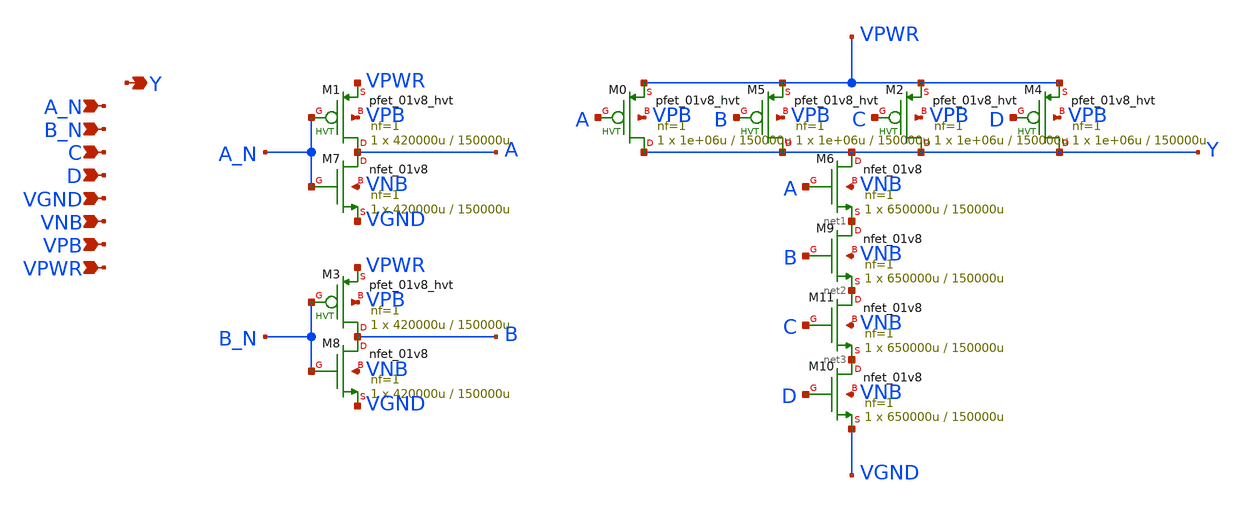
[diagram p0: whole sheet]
** sch_path: schematics/nand4bb/sky130_fd_sc_hd__nand4bb_1.sch
**.subckt sky130_fd_sc_hd__nand4bb_1 A_N B_N C D VGND VNB VPB VPWR Y
*.ipin A_N
*.ipin B_N
*.ipin C
*.ipin D
*.ipin VGND
*.ipin VNB
*.ipin VPB
*.ipin VPWR
*.opin Y
XM0 Y A VPWR VPB sky130_fd_pr__pfet_01v8_hvt L=150000u W=1e+06u nf=1 ad='int((1 + 1)/2) * 1e+06u / 1 * 0.29'
+ as='int((1 + 2)/2) * 1e+06u / 1 * 0.29' pd='2*int((1 + 1)/2) * (1e+06u / 1 + 0.29)' ps='2*int((1 + 2)/2) * (1e+06u / 1 + 0.29)'
+ nrd='0.29 / 1e+06u ' nrs='0.29 / 1e+06u ' sa=0 sb=0 sd=0 mult=1 m=1
XM1 A A_N VPWR VPB sky130_fd_pr__pfet_01v8_hvt L=150000u W=420000u nf=1 ad='int((1 + 1)/2) * 420000u / 1 * 0.29'
+ as='int((1 + 2)/2) * 420000u / 1 * 0.29' pd='2*int((1 + 1)/2) * (420000u / 1 + 0.29)' ps='2*int((1 + 2)/2) * (420000u / 1 + 0.29)'
+ nrd='0.29 / 420000u ' nrs='0.29 / 420000u ' sa=0 sb=0 sd=0 mult=1 m=1
XM2 Y C VPWR VPB sky130_fd_pr__pfet_01v8_hvt L=150000u W=1e+06u nf=1 ad='int((1 + 1)/2) * 1e+06u / 1 * 0.29'
+ as='int((1 + 2)/2) * 1e+06u / 1 * 0.29' pd='2*int((1 + 1)/2) * (1e+06u / 1 + 0.29)' ps='2*int((1 + 2)/2) * (1e+06u / 1 + 0.29)'
+ nrd='0.29 / 1e+06u ' nrs='0.29 / 1e+06u ' sa=0 sb=0 sd=0 mult=1 m=1
XM3 B B_N VPWR VPB sky130_fd_pr__pfet_01v8_hvt L=150000u W=420000u nf=1 ad='int((1 + 1)/2) * 420000u / 1 * 0.29'
+ as='int((1 + 2)/2) * 420000u / 1 * 0.29' pd='2*int((1 + 1)/2) * (420000u / 1 + 0.29)' ps='2*int((1 + 2)/2) * (420000u / 1 + 0.29)'
+ nrd='0.29 / 420000u ' nrs='0.29 / 420000u ' sa=0 sb=0 sd=0 mult=1 m=1
XM4 Y D VPWR VPB sky130_fd_pr__pfet_01v8_hvt L=150000u W=1e+06u nf=1 ad='int((1 + 1)/2) * 1e+06u / 1 * 0.29'
+ as='int((1 + 2)/2) * 1e+06u / 1 * 0.29' pd='2*int((1 + 1)/2) * (1e+06u / 1 + 0.29)' ps='2*int((1 + 2)/2) * (1e+06u / 1 + 0.29)'
+ nrd='0.29 / 1e+06u ' nrs='0.29 / 1e+06u ' sa=0 sb=0 sd=0 mult=1 m=1
XM5 Y B VPWR VPB sky130_fd_pr__pfet_01v8_hvt L=150000u W=1e+06u nf=1 ad='int((1 + 1)/2) * 1e+06u / 1 * 0.29'
+ as='int((1 + 2)/2) * 1e+06u / 1 * 0.29' pd='2*int((1 + 1)/2) * (1e+06u / 1 + 0.29)' ps='2*int((1 + 2)/2) * (1e+06u / 1 + 0.29)'
+ nrd='0.29 / 1e+06u ' nrs='0.29 / 1e+06u ' sa=0 sb=0 sd=0 mult=1 m=1
XM6 Y A net1 VNB sky130_fd_pr__nfet_01v8 L=150000u W=650000u nf=1 ad='int((1 + 1)/2) * 650000u / 1 * 0.29'
+ as='int((1 + 2)/2) * 650000u / 1 * 0.29' pd='2*int((1 + 1)/2) * (650000u / 1 + 0.29)' ps='2*int((1 + 2)/2) * (650000u / 1 + 0.29)'
+ nrd='0.29 / 650000u ' nrs='0.29 / 650000u ' sa=0 sb=0 sd=0 mult=1 m=1
XM7 A A_N VGND VNB sky130_fd_pr__nfet_01v8 L=150000u W=420000u nf=1 ad='int((1 + 1)/2) * 420000u / 1 * 0.29'
+ as='int((1 + 2)/2) * 420000u / 1 * 0.29' pd='2*int((1 + 1)/2) * (420000u / 1 + 0.29)' ps='2*int((1 + 2)/2) * (420000u / 1 + 0.29)'
+ nrd='0.29 / 420000u ' nrs='0.29 / 420000u ' sa=0 sb=0 sd=0 mult=1 m=1
XM8 B B_N VGND VNB sky130_fd_pr__nfet_01v8 L=150000u W=420000u nf=1 ad='int((1 + 1)/2) * 420000u / 1 * 0.29'
+ as='int((1 + 2)/2) * 420000u / 1 * 0.29' pd='2*int((1 + 1)/2) * (420000u / 1 + 0.29)' ps='2*int((1 + 2)/2) * (420000u / 1 + 0.29)'
+ nrd='0.29 / 420000u ' nrs='0.29 / 420000u ' sa=0 sb=0 sd=0 mult=1 m=1
XM9 net1 B net2 VNB sky130_fd_pr__nfet_01v8 L=150000u W=650000u nf=1 ad='int((1 + 1)/2) * 650000u / 1 * 0.29'
+ as='int((1 + 2)/2) * 650000u / 1 * 0.29' pd='2*int((1 + 1)/2) * (650000u / 1 + 0.29)' ps='2*int((1 + 2)/2) * (650000u / 1 + 0.29)'
+ nrd='0.29 / 650000u ' nrs='0.29 / 650000u ' sa=0 sb=0 sd=0 mult=1 m=1
XM10 net3 D VGND VNB sky130_fd_pr__nfet_01v8 L=150000u W=650000u nf=1 ad='int((1 + 1)/2) * 650000u / 1 * 0.29'
+ as='int((1 + 2)/2) * 650000u / 1 * 0.29' pd='2*int((1 + 1)/2) * (650000u / 1 + 0.29)' ps='2*int((1 + 2)/2) * (650000u / 1 + 0.29)'
+ nrd='0.29 / 650000u ' nrs='0.29 / 650000u ' sa=0 sb=0 sd=0 mult=1 m=1
XM11 net2 C net3 VNB sky130_fd_pr__nfet_01v8 L=150000u W=650000u nf=1 ad='int((1 + 1)/2) * 650000u / 1 * 0.29'
+ as='int((1 + 2)/2) * 650000u / 1 * 0.29' pd='2*int((1 + 1)/2) * (650000u / 1 + 0.29)' ps='2*int((1 + 2)/2) * (650000u / 1 + 0.29)'
+ nrd='0.29 / 650000u ' nrs='0.29 / 650000u ' sa=0 sb=0 sd=0 mult=1 m=1
**.ends
.end
